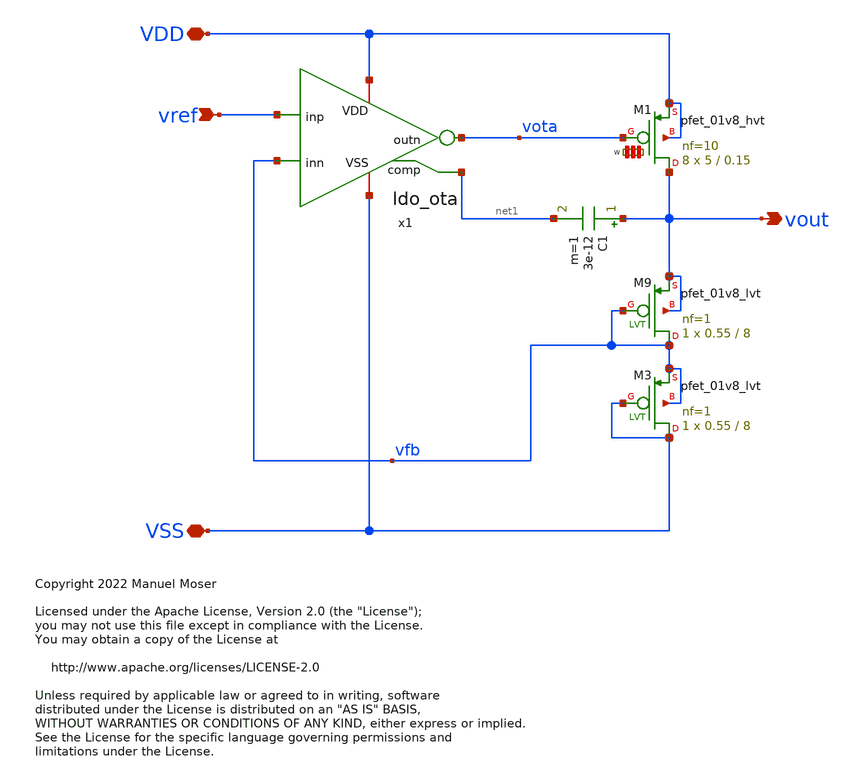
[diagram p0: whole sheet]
** sch_path: xschem/ldo.sch
* Copyright 2022 Manuel Moser
* Licensed under the Apache License, Version 2.0 (the "License");
**.subckt ldo vref VDD VSS vout
*.ipin vref
*.iopin VDD
*.iopin VSS
*.opin vout
x1 VDD vref vota vfb VSS net1 ldo_ota
XM1 vout vota VDD VDD sky130_fd_pr__pfet_01v8_hvt L=0.15 W='5 * 10 ' nf=10 ad='int((nf+1)/2) * W / nf * 0.29'
+ as='int((nf+2)/2) * W / nf * 0.29' pd='2*int((nf+1)/2) * (W / nf + 0.29)' ps='2*int((nf+2)/2) * (W / nf + 0.29)'
+ nrd='0.29 / W ' nrs='0.29 / W ' sa=0 sb=0 sd=0 mult=8 m=8
C1 vout net1 3e-12 m=1
XM9 vfb vfb vout vout sky130_fd_pr__pfet_01v8_lvt L=8 W=0.55 nf=1 ad='int((nf+1)/2) * W/nf * 0.29' as='int((nf+2)/2) * W/nf * 0.29'
+ pd='2*int((nf+1)/2) * (W/nf + 0.29)' ps='2*int((nf+2)/2) * (W/nf + 0.29)' nrd='0.29 / W' nrs='0.29 / W'
+ sa=0 sb=0 sd=0 mult=1 m=1
XM3 VSS VSS vfb vfb sky130_fd_pr__pfet_01v8_lvt L=8 W=0.55 nf=1 ad='int((nf+1)/2) * W/nf * 0.29' as='int((nf+2)/2) * W/nf * 0.29'
+ pd='2*int((nf+1)/2) * (W/nf + 0.29)' ps='2*int((nf+2)/2) * (W/nf + 0.29)' nrd='0.29 / W' nrs='0.29 / W'
+ sa=0 sb=0 sd=0 mult=1 m=1
**.ends

* expanding   symbol:  ldo_ota.sym # of pins=6
** sym_path: xschem/ldo_ota.sym
** sch_path: xschem/ldo_ota.sch
.subckt ldo_ota VDD inp outn inn VSS comp
*.iopin VDD
*.iopin VSS
*.ipin inp
*.ipin inn
*.opin outn
*.opin comp
x2 bias2 VDD VSS bias1 ldo_isource
XM10 net1 bias2 VDD VDD sky130_fd_pr__pfet_01v8_lvt L=8 W='0.55 * 1 ' nf=1 ad='int((nf+1)/2) * W / nf * 0.29'
+ as='int((nf+2)/2) * W / nf * 0.29' pd='2*int((nf+1)/2) * (W / nf + 0.29)' ps='2*int((nf+2)/2) * (W / nf + 0.29)'
+ nrd='0.29 / W ' nrs='0.29 / W ' sa=0 sb=0 sd=0 mult=1 m=1
XM12 bias2 bias2 net1 VDD sky130_fd_pr__pfet_01v8_lvt L=0.5 W='1 * 3 ' nf=3 ad='int((nf+1)/2) * W / nf * 0.29'
+ as='int((nf+2)/2) * W / nf * 0.29' pd='2*int((nf+1)/2) * (W / nf + 0.29)' ps='2*int((nf+2)/2) * (W / nf + 0.29)'
+ nrd='0.29 / W ' nrs='0.29 / W ' sa=0 sb=0 sd=0 mult=1 m=1
XM1 net2 bias1 VDD VDD sky130_fd_pr__pfet_01v8_lvt L=8 W='0.55 * 4 ' nf=4 ad='int((nf+1)/2) * W / nf * 0.29'
+ as='int((nf+2)/2) * W / nf * 0.29' pd='2*int((nf+1)/2) * (W / nf + 0.29)' ps='2*int((nf+2)/2) * (W / nf + 0.29)'
+ nrd='0.29 / W ' nrs='0.29 / W ' sa=0 sb=0 sd=0 mult=1 m=1
XM2 bias1 bias2 net2 VDD sky130_fd_pr__pfet_01v8_lvt L=0.5 W='1 * 3 ' nf=3 ad='int((nf+1)/2) * W / nf * 0.29'
+ as='int((nf+2)/2) * W / nf * 0.29' pd='2*int((nf+1)/2) * (W / nf + 0.29)' ps='2*int((nf+2)/2) * (W / nf + 0.29)'
+ nrd='0.29 / W ' nrs='0.29 / W ' sa=0 sb=0 sd=0 mult=1 m=1
XM3 net3 bias1 VDD VDD sky130_fd_pr__pfet_01v8_lvt L=8 W='0.55 * 4 ' nf=4 ad='int((nf+1)/2) * W / nf * 0.29'
+ as='int((nf+2)/2) * W / nf * 0.29' pd='2*int((nf+1)/2) * (W / nf + 0.29)' ps='2*int((nf+2)/2) * (W / nf + 0.29)'
+ nrd='0.29 / W ' nrs='0.29 / W ' sa=0 sb=0 sd=0 mult=1 m=1
XM4 bias3 bias2 net3 VDD sky130_fd_pr__pfet_01v8_lvt L=0.5 W='1 * 3 ' nf=3 ad='int((nf+1)/2) * W / nf * 0.29'
+ as='int((nf+2)/2) * W / nf * 0.29' pd='2*int((nf+1)/2) * (W / nf + 0.29)' ps='2*int((nf+2)/2) * (W / nf + 0.29)'
+ nrd='0.29 / W ' nrs='0.29 / W ' sa=0 sb=0 sd=0 mult=1 m=1
XM5 net4 bias1 VDD VDD sky130_fd_pr__pfet_01v8_lvt L=8 W='0.55 * 4 ' nf=4 ad='int((nf+1)/2) * W / nf * 0.29'
+ as='int((nf+2)/2) * W / nf * 0.29' pd='2*int((nf+1)/2) * (W / nf + 0.29)' ps='2*int((nf+2)/2) * (W / nf + 0.29)'
+ nrd='0.29 / W ' nrs='0.29 / W ' sa=0 sb=0 sd=0 mult=1 m=1
XM8 bias4 bias2 net4 VDD sky130_fd_pr__pfet_01v8_lvt L=0.5 W='1 * 3 ' nf=3 ad='int((nf+1)/2) * W / nf * 0.29'
+ as='int((nf+2)/2) * W / nf * 0.29' pd='2*int((nf+1)/2) * (W / nf + 0.29)' ps='2*int((nf+2)/2) * (W / nf + 0.29)'
+ nrd='0.29 / W ' nrs='0.29 / W ' sa=0 sb=0 sd=0 mult=1 m=1
XM9 bias3 bias3 net5 VSS sky130_fd_pr__nfet_01v8_lvt L=0.5 W='1 * 2 ' nf=2 ad='int((nf+1)/2) * W / nf * 0.29'
+ as='int((nf+2)/2) * W / nf * 0.29' pd='2*int((nf+1)/2) * (W / nf + 0.29)' ps='2*int((nf+2)/2) * (W / nf + 0.29)'
+ nrd='0.29 / W ' nrs='0.29 / W ' sa=0 sb=0 sd=0 mult=1 m=1
XM11 net5 bias3 net10 VSS sky130_fd_pr__nfet_01v8 L=8 W='0.42 * 1 ' nf=1 ad='int((nf+1)/2) * W / nf * 0.29'
+ as='int((nf+2)/2) * W / nf * 0.29' pd='2*int((nf+1)/2) * (W / nf + 0.29)' ps='2*int((nf+2)/2) * (W / nf + 0.29)'
+ nrd='0.29 / W ' nrs='0.29 / W ' sa=0 sb=0 sd=0 mult=1 m=1
XM13 bias4 bias3 net6 VSS sky130_fd_pr__nfet_01v8_lvt L=0.5 W='1 * 2 ' nf=2 ad='int((nf+1)/2) * W / nf * 0.29'
+ as='int((nf+2)/2) * W / nf * 0.29' pd='2*int((nf+1)/2) * (W / nf + 0.29)' ps='2*int((nf+2)/2) * (W / nf + 0.29)'
+ nrd='0.29 / W ' nrs='0.29 / W ' sa=0 sb=0 sd=0 mult=1 m=1
XM14 net6 bias4 net7 VSS sky130_fd_pr__nfet_01v8 L=8 W='0.42 * 4 ' nf=4 ad='int((nf+1)/2) * W / nf * 0.29'
+ as='int((nf+2)/2) * W / nf * 0.29' pd='2*int((nf+1)/2) * (W / nf + 0.29)' ps='2*int((nf+2)/2) * (W / nf + 0.29)'
+ nrd='0.29 / W ' nrs='0.29 / W ' sa=0 sb=0 sd=0 mult=1 m=1
XM6 net7 bias4 net8 VSS sky130_fd_pr__nfet_01v8 L=8 W='0.42 * 4 ' nf=4 ad='int((nf+1)/2) * W / nf * 0.29'
+ as='int((nf+2)/2) * W / nf * 0.29' pd='2*int((nf+1)/2) * (W / nf + 0.29)' ps='2*int((nf+2)/2) * (W / nf + 0.29)'
+ nrd='0.29 / W ' nrs='0.29 / W ' sa=0 sb=0 sd=0 mult=1 m=1
XM7 net10 bias3 net9 VSS sky130_fd_pr__nfet_01v8 L=8 W='0.42 * 1 ' nf=1 ad='int((nf+1)/2) * W / nf * 0.29'
+ as='int((nf+2)/2) * W / nf * 0.29' pd='2*int((nf+1)/2) * (W / nf + 0.29)' ps='2*int((nf+2)/2) * (W / nf + 0.29)'
+ nrd='0.29 / W ' nrs='0.29 / W ' sa=0 sb=0 sd=0 mult=1 m=1
x1 VDD inp inn bias1 bias2 bias3 outn VSS bias4 comp ldo_fc_n
XM15 net9 bias3 net11 VSS sky130_fd_pr__nfet_01v8 L=8 W='0.42 * 1 ' nf=1 ad='int((nf+1)/2) * W / nf * 0.29'
+ as='int((nf+2)/2) * W / nf * 0.29' pd='2*int((nf+1)/2) * (W / nf + 0.29)' ps='2*int((nf+2)/2) * (W / nf + 0.29)'
+ nrd='0.29 / W ' nrs='0.29 / W ' sa=0 sb=0 sd=0 mult=1 m=1
XM16 net8 bias4 net12 VSS sky130_fd_pr__nfet_01v8 L=8 W='0.42 * 4 ' nf=4 ad='int((nf+1)/2) * W / nf * 0.29'
+ as='int((nf+2)/2) * W / nf * 0.29' pd='2*int((nf+1)/2) * (W / nf + 0.29)' ps='2*int((nf+2)/2) * (W / nf + 0.29)'
+ nrd='0.29 / W ' nrs='0.29 / W ' sa=0 sb=0 sd=0 mult=1 m=1
XM17 net12 bias4 VSS VSS sky130_fd_pr__nfet_01v8 L=8 W='0.42 * 4 ' nf=4 ad='int((nf+1)/2) * W / nf * 0.29'
+ as='int((nf+2)/2) * W / nf * 0.29' pd='2*int((nf+1)/2) * (W / nf + 0.29)' ps='2*int((nf+2)/2) * (W / nf + 0.29)'
+ nrd='0.29 / W ' nrs='0.29 / W ' sa=0 sb=0 sd=0 mult=1 m=1
XM18 net11 bias3 VSS VSS sky130_fd_pr__nfet_01v8 L=8 W='0.42 * 1 ' nf=1 ad='int((nf+1)/2) * W / nf * 0.29'
+ as='int((nf+2)/2) * W / nf * 0.29' pd='2*int((nf+1)/2) * (W / nf + 0.29)' ps='2*int((nf+2)/2) * (W / nf + 0.29)'
+ nrd='0.29 / W ' nrs='0.29 / W ' sa=0 sb=0 sd=0 mult=1 m=1
.ends


* expanding   symbol:  ldo_isource.sym # of pins=4
** sym_path: xschem/ldo_isource.sym
** sch_path: xschem/ldo_isource.sch
.subckt ldo_isource curr_n1 VDD VSS curr_n2
*.iopin VDD
*.iopin VSS
*.ipin curr_n1
*.ipin curr_n2
XMP2 VGP VGP net4 VDD sky130_fd_pr__pfet_01v8_lvt L=8 W='0.55 * 7 ' nf=7 ad='int((nf+1)/2) * W / nf * 0.29'
+ as='int((nf+2)/2) * W / nf * 0.29' pd='2*int((nf+1)/2) * (W / nf + 0.29)' ps='2*int((nf+2)/2) * (W / nf + 0.29)'
+ nrd='0.29 / W ' nrs='0.29 / W ' sa=0 sb=0 sd=0 mult=1 m=1
XMP1 VGN VGP net3 VDD sky130_fd_pr__pfet_01v8_lvt L=8 W='0.55 * 7 ' nf=7 ad='int((nf+1)/2) * W / nf * 0.29'
+ as='int((nf+2)/2) * W / nf * 0.29' pd='2*int((nf+1)/2) * (W / nf + 0.29)' ps='2*int((nf+2)/2) * (W / nf + 0.29)'
+ nrd='0.29 / W ' nrs='0.29 / W ' sa=0 sb=0 sd=0 mult=1 m=1
XMN1 VGN VGN net1 VSS sky130_fd_pr__nfet_01v8_lvt L=8 W='7 * 1 ' nf=1 ad='int((nf+1)/2) * W / nf * 0.29'
+ as='int((nf+2)/2) * W / nf * 0.29' pd='2*int((nf+1)/2) * (W / nf + 0.29)' ps='2*int((nf+2)/2) * (W / nf + 0.29)'
+ nrd='0.29 / W ' nrs='0.29 / W ' sa=0 sb=0 sd=0 mult=1 m=1
XMN2 VGP VGN net2 VSS sky130_fd_pr__nfet_01v8_lvt L=8 W='7 * 1 ' nf=1 ad='int((nf+1)/2) * W / nf * 0.29'
+ as='int((nf+2)/2) * W / nf * 0.29' pd='2*int((nf+1)/2) * (W / nf + 0.29)' ps='2*int((nf+2)/2) * (W / nf + 0.29)'
+ nrd='0.29 / W ' nrs='0.29 / W ' sa=0 sb=0 sd=0 mult=5 m=5
XMN3 net1 VGN VSS VSS sky130_fd_pr__nfet_01v8_lvt L=8 W='7 * 1 ' nf=1 ad='int((nf+1)/2) * W / nf * 0.29'
+ as='int((nf+2)/2) * W / nf * 0.29' pd='2*int((nf+1)/2) * (W / nf + 0.29)' ps='2*int((nf+2)/2) * (W / nf + 0.29)'
+ nrd='0.29 / W ' nrs='0.29 / W ' sa=0 sb=0 sd=0 mult=1 m=1
XMN4 net2 VGN Vref VSS sky130_fd_pr__nfet_01v8_lvt L=8 W='7 * 1 ' nf=1 ad='int((nf+1)/2) * W / nf * 0.29'
+ as='int((nf+2)/2) * W / nf * 0.29' pd='2*int((nf+1)/2) * (W / nf + 0.29)' ps='2*int((nf+2)/2) * (W / nf + 0.29)'
+ nrd='0.29 / W ' nrs='0.29 / W ' sa=0 sb=0 sd=0 mult=5 m=5
XMP4 net3 VGP VDD VDD sky130_fd_pr__pfet_01v8_lvt L=8 W='0.55 * 7 ' nf=7 ad='int((nf+1)/2) * W / nf * 0.29'
+ as='int((nf+2)/2) * W / nf * 0.29' pd='2*int((nf+1)/2) * (W / nf + 0.29)' ps='2*int((nf+2)/2) * (W / nf + 0.29)'
+ nrd='0.29 / W ' nrs='0.29 / W ' sa=0 sb=0 sd=0 mult=1 m=1
XMP5 net4 VGP VDD VDD sky130_fd_pr__pfet_01v8_lvt L=8 W='0.55 * 7 ' nf=7 ad='int((nf+1)/2) * W / nf * 0.29'
+ as='int((nf+2)/2) * W / nf * 0.29' pd='2*int((nf+1)/2) * (W / nf + 0.29)' ps='2*int((nf+2)/2) * (W / nf + 0.29)'
+ nrd='0.29 / W ' nrs='0.29 / W ' sa=0 sb=0 sd=0 mult=1 m=1
XMP3 Vrefgate VGP net19 VDD sky130_fd_pr__pfet_01v8_lvt L=8 W='0.55 * 7 ' nf=7 ad='int((nf+1)/2) * W / nf * 0.29'
+ as='int((nf+2)/2) * W / nf * 0.29' pd='2*int((nf+1)/2) * (W / nf + 0.29)' ps='2*int((nf+2)/2) * (W / nf + 0.29)'
+ nrd='0.29 / W ' nrs='0.29 / W ' sa=0 sb=0 sd=0 mult=1 m=1
XM2 net5 Vrefgate net6 VSS sky130_fd_pr__nfet_01v8 L=4 W='1 * 1 ' nf=1 ad='int((nf+1)/2) * W / nf * 0.29'
+ as='int((nf+2)/2) * W / nf * 0.29' pd='2*int((nf+1)/2) * (W / nf + 0.29)' ps='2*int((nf+2)/2) * (W / nf + 0.29)'
+ nrd='0.29 / W ' nrs='0.29 / W ' sa=0 sb=0 sd=0 mult=1 m=1
XM3 net8 Vrefgate VSS VSS sky130_fd_pr__nfet_01v8 L=4 W='1 * 1 ' nf=1 ad='int((nf+1)/2) * W / nf * 0.29'
+ as='int((nf+2)/2) * W / nf * 0.29' pd='2*int((nf+1)/2) * (W / nf + 0.29)' ps='2*int((nf+2)/2) * (W / nf + 0.29)'
+ nrd='0.29 / W ' nrs='0.29 / W ' sa=0 sb=0 sd=0 mult=1 m=1
XM1 net7 Vrefgate net8 VSS sky130_fd_pr__nfet_01v8 L=4 W='1 * 1 ' nf=1 ad='int((nf+1)/2) * W / nf * 0.29'
+ as='int((nf+2)/2) * W / nf * 0.29' pd='2*int((nf+1)/2) * (W / nf + 0.29)' ps='2*int((nf+2)/2) * (W / nf + 0.29)'
+ nrd='0.29 / W ' nrs='0.29 / W ' sa=0 sb=0 sd=0 mult=1 m=1
XM4 net6 Vrefgate net7 VSS sky130_fd_pr__nfet_01v8 L=4 W='1 * 1 ' nf=1 ad='int((nf+1)/2) * W / nf * 0.29'
+ as='int((nf+2)/2) * W / nf * 0.29' pd='2*int((nf+1)/2) * (W / nf + 0.29)' ps='2*int((nf+2)/2) * (W / nf + 0.29)'
+ nrd='0.29 / W ' nrs='0.29 / W ' sa=0 sb=0 sd=0 mult=1 m=1
XMN5 net10 Vrefgate VSS VSS sky130_fd_pr__nfet_01v8_lvt L=4 W='1 * 1 ' nf=1 ad='int((nf+1)/2) * W / nf * 0.29'
+ as='int((nf+2)/2) * W / nf * 0.29' pd='2*int((nf+1)/2) * (W / nf + 0.29)' ps='2*int((nf+2)/2) * (W / nf + 0.29)'
+ nrd='0.29 / W ' nrs='0.29 / W ' sa=0 sb=0 sd=0 mult=1 m=1
XMN6 net14 Vrefgate net9 VSS sky130_fd_pr__nfet_01v8_lvt L=4 W='1 * 1 ' nf=1 ad='int((nf+1)/2) * W / nf * 0.29'
+ as='int((nf+2)/2) * W / nf * 0.29' pd='2*int((nf+1)/2) * (W / nf + 0.29)' ps='2*int((nf+2)/2) * (W / nf + 0.29)'
+ nrd='0.29 / W ' nrs='0.29 / W ' sa=0 sb=0 sd=0 mult=1 m=1
XMN9 net16 Vrefgate net14 VSS sky130_fd_pr__nfet_01v8_lvt L=4 W='1 * 1 ' nf=1 ad='int((nf+1)/2) * W / nf * 0.29'
+ as='int((nf+2)/2) * W / nf * 0.29' pd='2*int((nf+1)/2) * (W / nf + 0.29)' ps='2*int((nf+2)/2) * (W / nf + 0.29)'
+ nrd='0.29 / W ' nrs='0.29 / W ' sa=0 sb=0 sd=0 mult=1 m=1
XM5 Vrefgate Vrefgate net5 VSS sky130_fd_pr__nfet_01v8 L=4 W='1 * 1 ' nf=1 ad='int((nf+1)/2) * W / nf * 0.29'
+ as='int((nf+2)/2) * W / nf * 0.29' pd='2*int((nf+1)/2) * (W / nf + 0.29)' ps='2*int((nf+2)/2) * (W / nf + 0.29)'
+ nrd='0.29 / W ' nrs='0.29 / W ' sa=0 sb=0 sd=0 mult=1 m=1
XMN10 net11 Vrefgate net10 VSS sky130_fd_pr__nfet_01v8_lvt L=4 W='1 * 1 ' nf=1 ad='int((nf+1)/2) * W / nf * 0.29'
+ as='int((nf+2)/2) * W / nf * 0.29' pd='2*int((nf+1)/2) * (W / nf + 0.29)' ps='2*int((nf+2)/2) * (W / nf + 0.29)'
+ nrd='0.29 / W ' nrs='0.29 / W ' sa=0 sb=0 sd=0 mult=1 m=1
XMN11 net12 Vrefgate net11 VSS sky130_fd_pr__nfet_01v8_lvt L=4 W='1 * 1 ' nf=1 ad='int((nf+1)/2) * W / nf * 0.29'
+ as='int((nf+2)/2) * W / nf * 0.29' pd='2*int((nf+1)/2) * (W / nf + 0.29)' ps='2*int((nf+2)/2) * (W / nf + 0.29)'
+ nrd='0.29 / W ' nrs='0.29 / W ' sa=0 sb=0 sd=0 mult=1 m=1
XMN12 net13 Vrefgate net12 VSS sky130_fd_pr__nfet_01v8_lvt L=4 W='1 * 1 ' nf=1 ad='int((nf+1)/2) * W / nf * 0.29'
+ as='int((nf+2)/2) * W / nf * 0.29' pd='2*int((nf+1)/2) * (W / nf + 0.29)' ps='2*int((nf+2)/2) * (W / nf + 0.29)'
+ nrd='0.29 / W ' nrs='0.29 / W ' sa=0 sb=0 sd=0 mult=1 m=1
XMN13 net9 Vrefgate net13 VSS sky130_fd_pr__nfet_01v8_lvt L=4 W='1 * 1 ' nf=1 ad='int((nf+1)/2) * W / nf * 0.29'
+ as='int((nf+2)/2) * W / nf * 0.29' pd='2*int((nf+1)/2) * (W / nf + 0.29)' ps='2*int((nf+2)/2) * (W / nf + 0.29)'
+ nrd='0.29 / W ' nrs='0.29 / W ' sa=0 sb=0 sd=0 mult=1 m=1
XMN7 net18 Vrefgate net15 VSS sky130_fd_pr__nfet_01v8_lvt L=4 W='1 * 1 ' nf=1 ad='int((nf+1)/2) * W / nf * 0.29'
+ as='int((nf+2)/2) * W / nf * 0.29' pd='2*int((nf+1)/2) * (W / nf + 0.29)' ps='2*int((nf+2)/2) * (W / nf + 0.29)'
+ nrd='0.29 / W ' nrs='0.29 / W ' sa=0 sb=0 sd=0 mult=1 m=1
XMN8 Vref Vrefgate net18 VSS sky130_fd_pr__nfet_01v8_lvt L=4 W='1 * 1 ' nf=1 ad='int((nf+1)/2) * W / nf * 0.29'
+ as='int((nf+2)/2) * W / nf * 0.29' pd='2*int((nf+1)/2) * (W / nf + 0.29)' ps='2*int((nf+2)/2) * (W / nf + 0.29)'
+ nrd='0.29 / W ' nrs='0.29 / W ' sa=0 sb=0 sd=0 mult=1 m=1
XMN14 net17 Vrefgate net16 VSS sky130_fd_pr__nfet_01v8_lvt L=4 W='1 * 1 ' nf=1 ad='int((nf+1)/2) * W / nf * 0.29'
+ as='int((nf+2)/2) * W / nf * 0.29' pd='2*int((nf+1)/2) * (W / nf + 0.29)' ps='2*int((nf+2)/2) * (W / nf + 0.29)'
+ nrd='0.29 / W ' nrs='0.29 / W ' sa=0 sb=0 sd=0 mult=1 m=1
XMN15 net15 Vrefgate net17 VSS sky130_fd_pr__nfet_01v8_lvt L=4 W='1 * 1 ' nf=1 ad='int((nf+1)/2) * W / nf * 0.29'
+ as='int((nf+2)/2) * W / nf * 0.29' pd='2*int((nf+1)/2) * (W / nf + 0.29)' ps='2*int((nf+2)/2) * (W / nf + 0.29)'
+ nrd='0.29 / W ' nrs='0.29 / W ' sa=0 sb=0 sd=0 mult=1 m=1
XMP6 net19 VGP VDD VDD sky130_fd_pr__pfet_01v8_lvt L=8 W='0.55 * 7 ' nf=7 ad='int((nf+1)/2) * W / nf * 0.29'
+ as='int((nf+2)/2) * W / nf * 0.29' pd='2*int((nf+1)/2) * (W / nf + 0.29)' ps='2*int((nf+2)/2) * (W / nf + 0.29)'
+ nrd='0.29 / W ' nrs='0.29 / W ' sa=0 sb=0 sd=0 mult=1 m=1
XMN16 curr_n1 VGN net20 VSS sky130_fd_pr__nfet_01v8_lvt L=8 W='7 * 1 ' nf=1 ad='int((nf+1)/2) * W / nf * 0.29'
+ as='int((nf+2)/2) * W / nf * 0.29' pd='2*int((nf+1)/2) * (W / nf + 0.29)' ps='2*int((nf+2)/2) * (W / nf + 0.29)'
+ nrd='0.29 / W ' nrs='0.29 / W ' sa=0 sb=0 sd=0 mult=1 m=1
XMN17 net20 VGN VSS VSS sky130_fd_pr__nfet_01v8_lvt L=8 W='7 * 1 ' nf=1 ad='int((nf+1)/2) * W / nf * 0.29'
+ as='int((nf+2)/2) * W / nf * 0.29' pd='2*int((nf+1)/2) * (W / nf + 0.29)' ps='2*int((nf+2)/2) * (W / nf + 0.29)'
+ nrd='0.29 / W ' nrs='0.29 / W ' sa=0 sb=0 sd=0 mult=1 m=1
XM6 VGP vstartup VGN VSS sky130_fd_pr__nfet_01v8 L=4 W='1 * 1 ' nf=1 ad='int((nf+1)/2) * W / nf * 0.29'
+ as='int((nf+2)/2) * W / nf * 0.29' pd='2*int((nf+1)/2) * (W / nf + 0.29)' ps='2*int((nf+2)/2) * (W / nf + 0.29)'
+ nrd='0.29 / W ' nrs='0.29 / W ' sa=0 sb=0 sd=0 mult=1 m=1
XM7 vstartup Vrefgate VSS VSS sky130_fd_pr__nfet_01v8 L=4 W='1 * 1 ' nf=1 ad='int((nf+1)/2) * W / nf * 0.29'
+ as='int((nf+2)/2) * W / nf * 0.29' pd='2*int((nf+1)/2) * (W / nf + 0.29)' ps='2*int((nf+2)/2) * (W / nf + 0.29)'
+ nrd='0.29 / W ' nrs='0.29 / W ' sa=0 sb=0 sd=0 mult=1 m=1
XMN18 curr_n2 VGN net21 VSS sky130_fd_pr__nfet_01v8_lvt L=8 W='7 * 1 ' nf=1 ad='int((nf+1)/2) * W / nf * 0.29'
+ as='int((nf+2)/2) * W / nf * 0.29' pd='2*int((nf+1)/2) * (W / nf + 0.29)' ps='2*int((nf+2)/2) * (W / nf + 0.29)'
+ nrd='0.29 / W ' nrs='0.29 / W ' sa=0 sb=0 sd=0 mult=1 m=1
XMN19 net21 VGN VSS VSS sky130_fd_pr__nfet_01v8_lvt L=8 W='7 * 1 ' nf=1 ad='int((nf+1)/2) * W / nf * 0.29'
+ as='int((nf+2)/2) * W / nf * 0.29' pd='2*int((nf+1)/2) * (W / nf + 0.29)' ps='2*int((nf+2)/2) * (W / nf + 0.29)'
+ nrd='0.29 / W ' nrs='0.29 / W ' sa=0 sb=0 sd=0 mult=1 m=1
XC1 VDD vstartup sky130_fd_pr__cap_mim_m3_2 W=4 L=4 MF=1 m=1
.ends


* expanding   symbol:  ldo_fc_n.sym # of pins=10
** sym_path: xschem/ldo_fc_n.sym
** sch_path: xschem/ldo_fc_n.sch
.subckt ldo_fc_n VDD inp inn bias1 bias2 bias3 outn VSS bias4 comp
*.iopin VSS
*.iopin VDD
*.ipin inp
*.ipin inn
*.ipin bias1
*.opin outn
*.ipin bias2
*.ipin bias3
*.ipin bias4
*.opin comp
XMN4 outn bias3 net1 VSS sky130_fd_pr__nfet_01v8_lvt L=0.5 W='1 * 2 ' nf=2 ad='int((nf+1)/2) * W / nf * 0.29'
+ as='int((nf+2)/2) * W / nf * 0.29' pd='2*int((nf+1)/2) * (W / nf + 0.29)' ps='2*int((nf+2)/2) * (W / nf + 0.29)'
+ nrd='0.29 / W ' nrs='0.29 / W ' sa=0 sb=0 sd=0 mult=7 m=7
XMN7 net1 net3 net7 VSS sky130_fd_pr__nfet_01v8 L=8 W='0.42 * 4 ' nf=4 ad='int((nf+1)/2) * W / nf * 0.29'
+ as='int((nf+2)/2) * W / nf * 0.29' pd='2*int((nf+1)/2) * (W / nf + 0.29)' ps='2*int((nf+2)/2) * (W / nf + 0.29)'
+ nrd='0.29 / W ' nrs='0.29 / W ' sa=0 sb=0 sd=0 mult=7 m=7
XMN3 net3 bias3 net2 VSS sky130_fd_pr__nfet_01v8_lvt L=0.5 W='1 * 2 ' nf=2 ad='int((nf+1)/2) * W / nf * 0.29'
+ as='int((nf+2)/2) * W / nf * 0.29' pd='2*int((nf+1)/2) * (W / nf + 0.29)' ps='2*int((nf+2)/2) * (W / nf + 0.29)'
+ nrd='0.29 / W ' nrs='0.29 / W ' sa=0 sb=0 sd=0 mult=7 m=7
XMN6 net2 net3 net6 VSS sky130_fd_pr__nfet_01v8 L=8 W='0.42 * 4 ' nf=4 ad='int((nf+1)/2) * W / nf * 0.29'
+ as='int((nf+2)/2) * W / nf * 0.29' pd='2*int((nf+1)/2) * (W / nf + 0.29)' ps='2*int((nf+2)/2) * (W / nf + 0.29)'
+ nrd='0.29 / W ' nrs='0.29 / W ' sa=0 sb=0 sd=0 mult=7 m=7
XMP4 outn bias2 comp VDD sky130_fd_pr__pfet_01v8_lvt L=0.5 W='1 * 3 ' nf=3 ad='int((nf+1)/2) * W / nf * 0.29'
+ as='int((nf+2)/2) * W / nf * 0.29' pd='2*int((nf+1)/2) * (W / nf + 0.29)' ps='2*int((nf+2)/2) * (W / nf + 0.29)'
+ nrd='0.29 / W ' nrs='0.29 / W ' sa=0 sb=0 sd=0 mult=7 m=7
XMP2 comp bias1 VDD VDD sky130_fd_pr__pfet_01v8_lvt L=8 W='0.55 * 4 ' nf=4 ad='int((nf+1)/2) * W / nf * 0.29'
+ as='int((nf+2)/2) * W / nf * 0.29' pd='2*int((nf+1)/2) * (W / nf + 0.29)' ps='2*int((nf+2)/2) * (W / nf + 0.29)'
+ nrd='0.29 / W ' nrs='0.29 / W ' sa=0 sb=0 sd=0 mult=11 m=11
XMP3 net3 bias2 net4 VDD sky130_fd_pr__pfet_01v8_lvt L=0.5 W='1 * 3 ' nf=3 ad='int((nf+1)/2) * W / nf * 0.29'
+ as='int((nf+2)/2) * W / nf * 0.29' pd='2*int((nf+1)/2) * (W / nf + 0.29)' ps='2*int((nf+2)/2) * (W / nf + 0.29)'
+ nrd='0.29 / W ' nrs='0.29 / W ' sa=0 sb=0 sd=0 mult=7 m=7
XMP1 net4 bias1 VDD VDD sky130_fd_pr__pfet_01v8_lvt L=8 W='0.55 * 4 ' nf=4 ad='int((nf+1)/2) * W / nf * 0.29'
+ as='int((nf+2)/2) * W / nf * 0.29' pd='2*int((nf+1)/2) * (W / nf + 0.29)' ps='2*int((nf+2)/2) * (W / nf + 0.29)'
+ nrd='0.29 / W ' nrs='0.29 / W ' sa=0 sb=0 sd=0 mult=11 m=11
XMN5 net5 bias4 net8 VSS sky130_fd_pr__nfet_01v8 L=8 W='0.42 * 4 ' nf=4 ad='int((nf+1)/2) * W / nf * 0.29'
+ as='int((nf+2)/2) * W / nf * 0.29' pd='2*int((nf+1)/2) * (W / nf + 0.29)' ps='2*int((nf+2)/2) * (W / nf + 0.29)'
+ nrd='0.29 / W ' nrs='0.29 / W ' sa=0 sb=0 sd=0 mult=8 m=8
XMN1 net4 inn net5 VSS sky130_fd_pr__nfet_01v8_lvt L=0.5 W='1 * 5 ' nf=5 ad='int((nf+1)/2) * W / nf * 0.29'
+ as='int((nf+2)/2) * W / nf * 0.29' pd='2*int((nf+1)/2) * (W / nf + 0.29)' ps='2*int((nf+2)/2) * (W / nf + 0.29)'
+ nrd='0.29 / W ' nrs='0.29 / W ' sa=0 sb=0 sd=0 mult=1 m=1
XMN2 comp inp net5 VSS sky130_fd_pr__nfet_01v8_lvt L=0.5 W='1 * 5 ' nf=5 ad='int((nf+1)/2) * W / nf * 0.29'
+ as='int((nf+2)/2) * W / nf * 0.29' pd='2*int((nf+1)/2) * (W / nf + 0.29)' ps='2*int((nf+2)/2) * (W / nf + 0.29)'
+ nrd='0.29 / W ' nrs='0.29 / W ' sa=0 sb=0 sd=0 mult=1 m=1
XMN9 net7 net3 net9 VSS sky130_fd_pr__nfet_01v8 L=8 W='0.42 * 4 ' nf=4 ad='int((nf+1)/2) * W / nf * 0.29'
+ as='int((nf+2)/2) * W / nf * 0.29' pd='2*int((nf+1)/2) * (W / nf + 0.29)' ps='2*int((nf+2)/2) * (W / nf + 0.29)'
+ nrd='0.29 / W ' nrs='0.29 / W ' sa=0 sb=0 sd=0 mult=7 m=7
XMN10 net6 net3 net10 VSS sky130_fd_pr__nfet_01v8 L=8 W='0.42 * 4 ' nf=4 ad='int((nf+1)/2) * W / nf * 0.29'
+ as='int((nf+2)/2) * W / nf * 0.29' pd='2*int((nf+1)/2) * (W / nf + 0.29)' ps='2*int((nf+2)/2) * (W / nf + 0.29)'
+ nrd='0.29 / W ' nrs='0.29 / W ' sa=0 sb=0 sd=0 mult=7 m=7
XMN11 net8 bias4 net11 VSS sky130_fd_pr__nfet_01v8 L=8 W='0.42 * 4 ' nf=4 ad='int((nf+1)/2) * W / nf * 0.29'
+ as='int((nf+2)/2) * W / nf * 0.29' pd='2*int((nf+1)/2) * (W / nf + 0.29)' ps='2*int((nf+2)/2) * (W / nf + 0.29)'
+ nrd='0.29 / W ' nrs='0.29 / W ' sa=0 sb=0 sd=0 mult=8 m=8
XMN8 net9 net3 net12 VSS sky130_fd_pr__nfet_01v8 L=8 W='0.42 * 4 ' nf=4 ad='int((nf+1)/2) * W / nf * 0.29'
+ as='int((nf+2)/2) * W / nf * 0.29' pd='2*int((nf+1)/2) * (W / nf + 0.29)' ps='2*int((nf+2)/2) * (W / nf + 0.29)'
+ nrd='0.29 / W ' nrs='0.29 / W ' sa=0 sb=0 sd=0 mult=7 m=7
XMN12 net10 net3 net14 VSS sky130_fd_pr__nfet_01v8 L=8 W='0.42 * 4 ' nf=4 ad='int((nf+1)/2) * W / nf * 0.29'
+ as='int((nf+2)/2) * W / nf * 0.29' pd='2*int((nf+1)/2) * (W / nf + 0.29)' ps='2*int((nf+2)/2) * (W / nf + 0.29)'
+ nrd='0.29 / W ' nrs='0.29 / W ' sa=0 sb=0 sd=0 mult=7 m=7
XMN13 net11 bias4 net13 VSS sky130_fd_pr__nfet_01v8 L=8 W='0.42 * 4 ' nf=4 ad='int((nf+1)/2) * W / nf * 0.29'
+ as='int((nf+2)/2) * W / nf * 0.29' pd='2*int((nf+1)/2) * (W / nf + 0.29)' ps='2*int((nf+2)/2) * (W / nf + 0.29)'
+ nrd='0.29 / W ' nrs='0.29 / W ' sa=0 sb=0 sd=0 mult=8 m=8
XMN14 net12 net3 VSS VSS sky130_fd_pr__nfet_01v8 L=8 W='0.42 * 4 ' nf=4 ad='int((nf+1)/2) * W / nf * 0.29'
+ as='int((nf+2)/2) * W / nf * 0.29' pd='2*int((nf+1)/2) * (W / nf + 0.29)' ps='2*int((nf+2)/2) * (W / nf + 0.29)'
+ nrd='0.29 / W ' nrs='0.29 / W ' sa=0 sb=0 sd=0 mult=7 m=7
XMN15 net14 net3 VSS VSS sky130_fd_pr__nfet_01v8 L=8 W='0.42 * 4 ' nf=4 ad='int((nf+1)/2) * W / nf * 0.29'
+ as='int((nf+2)/2) * W / nf * 0.29' pd='2*int((nf+1)/2) * (W / nf + 0.29)' ps='2*int((nf+2)/2) * (W / nf + 0.29)'
+ nrd='0.29 / W ' nrs='0.29 / W ' sa=0 sb=0 sd=0 mult=7 m=7
XMN16 net13 bias4 VSS VSS sky130_fd_pr__nfet_01v8 L=8 W='0.42 * 4 ' nf=4 ad='int((nf+1)/2) * W / nf * 0.29'
+ as='int((nf+2)/2) * W / nf * 0.29' pd='2*int((nf+1)/2) * (W / nf + 0.29)' ps='2*int((nf+2)/2) * (W / nf + 0.29)'
+ nrd='0.29 / W ' nrs='0.29 / W ' sa=0 sb=0 sd=0 mult=8 m=8
.ends

.end
